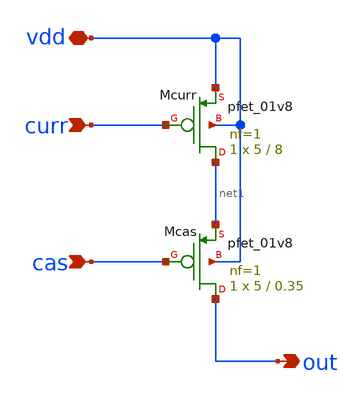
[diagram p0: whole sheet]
** sch_path: design/bandgap_cascurr_cell/bandgap_cascurr_cell.sch
**.subckt bandgap_cascurr_cell vdd curr cas out
*.iopin vdd
*.ipin curr
*.ipin cas
*.opin out
XMcurr net1 curr vdd vdd sky130_fd_pr__pfet_01v8 L=8 W=5 nf=1 ad='W * 0.29' as='W * 0.29' pd='2 * (W + 0.29)'
+ ps='2 * (W + 0.29)' nrd='0.29 / W' nrs='0.29 / W' sa=0 sb=0 sd=0 mult=1 m=1
XMcas out cas net1 vdd sky130_fd_pr__pfet_01v8 L=0.35 W=5 nf=1 ad='W * 0.29' as='W * 0.29' pd='2 * (W + 0.29)'
+ ps='2 * (W + 0.29)' nrd='0.29 / W' nrs='0.29 / W' sa=0 sb=0 sd=0 mult=1 m=1
**.ends
.end
